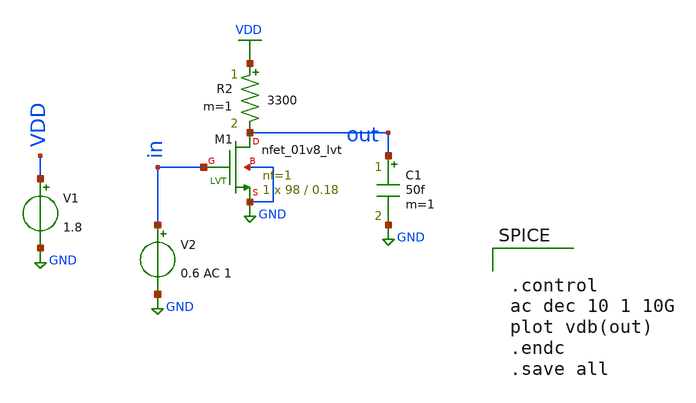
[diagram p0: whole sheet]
** sch_path: #2_cs_1ghz_gmid/cs1ghz_gmID.sch
**.subckt cs1ghz_gmID
V1 VDD GND 1.8
R2 VDD out 3300 m=1
V2 in GND 0.6 AC 1
C1 out GND 50f m=1
XM1 out in GND GND sky130_fd_pr__nfet_01v8_lvt L=0.18 W=98 nf=1 ad='int((nf+1)/2) * W/nf * 0.29' as='int((nf+2)/2) * W/nf * 0.29'
+ pd='2*int((nf+1)/2) * (W/nf + 0.29)' ps='2*int((nf+2)/2) * (W/nf + 0.29)' nrd='0.29 / W' nrs='0.29 / W'
+ sa=0 sb=0 sd=0 mult=1 m=1
**** begin user architecture code

** opencircuitdesign pdks install
.lib $::SKYWATER_MODELS/sky130.lib.spice tt




.control
ac dec 10 1 10G
plot vdb(out)
.endc
.save all


**** end user architecture code
**.ends
.GLOBAL GND
.GLOBAL VDD
.end
